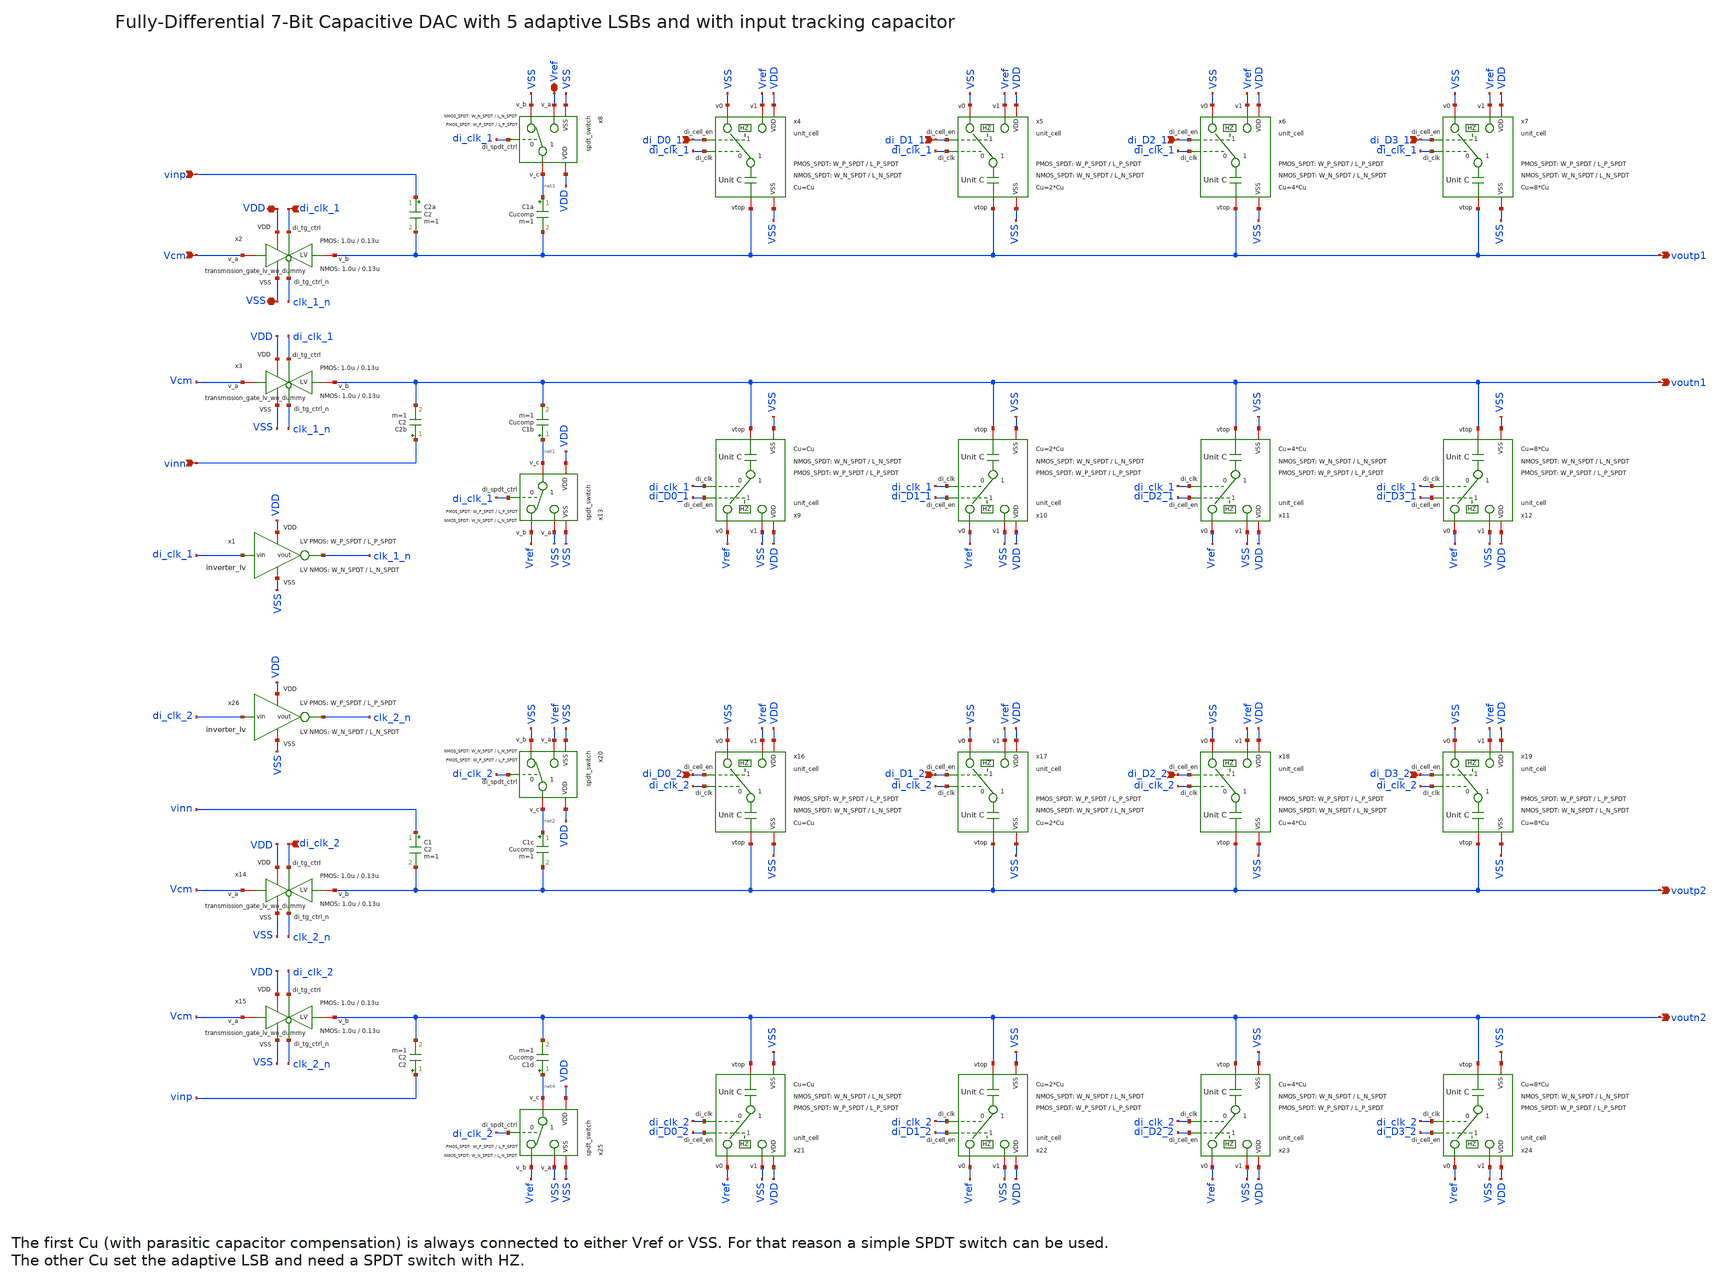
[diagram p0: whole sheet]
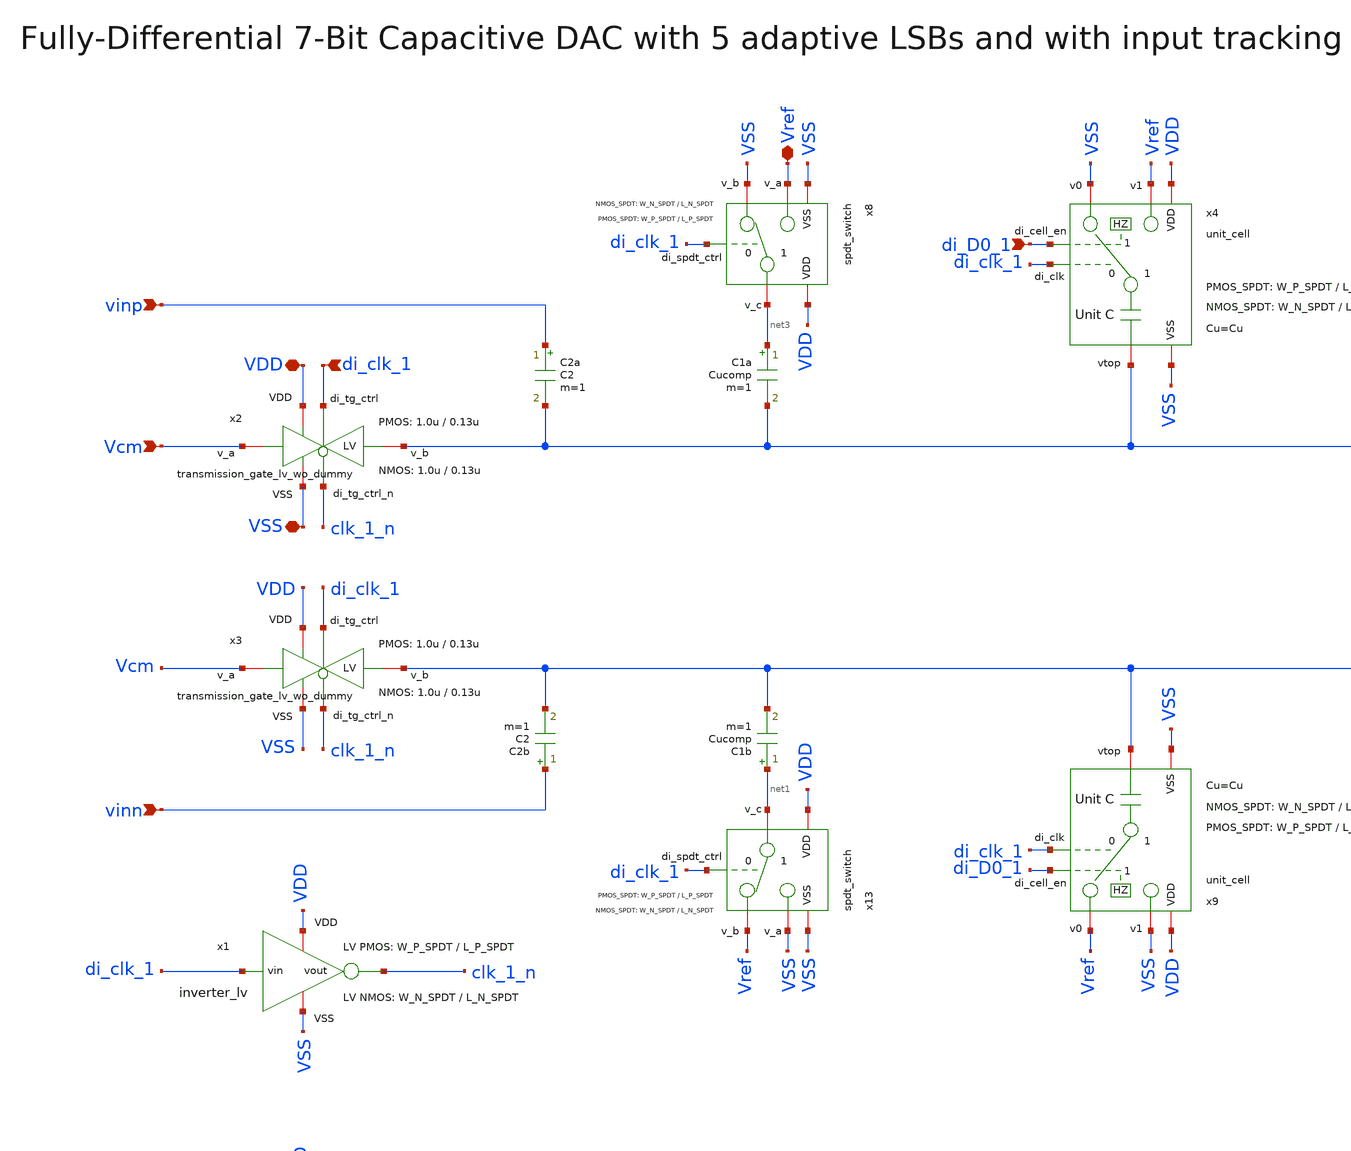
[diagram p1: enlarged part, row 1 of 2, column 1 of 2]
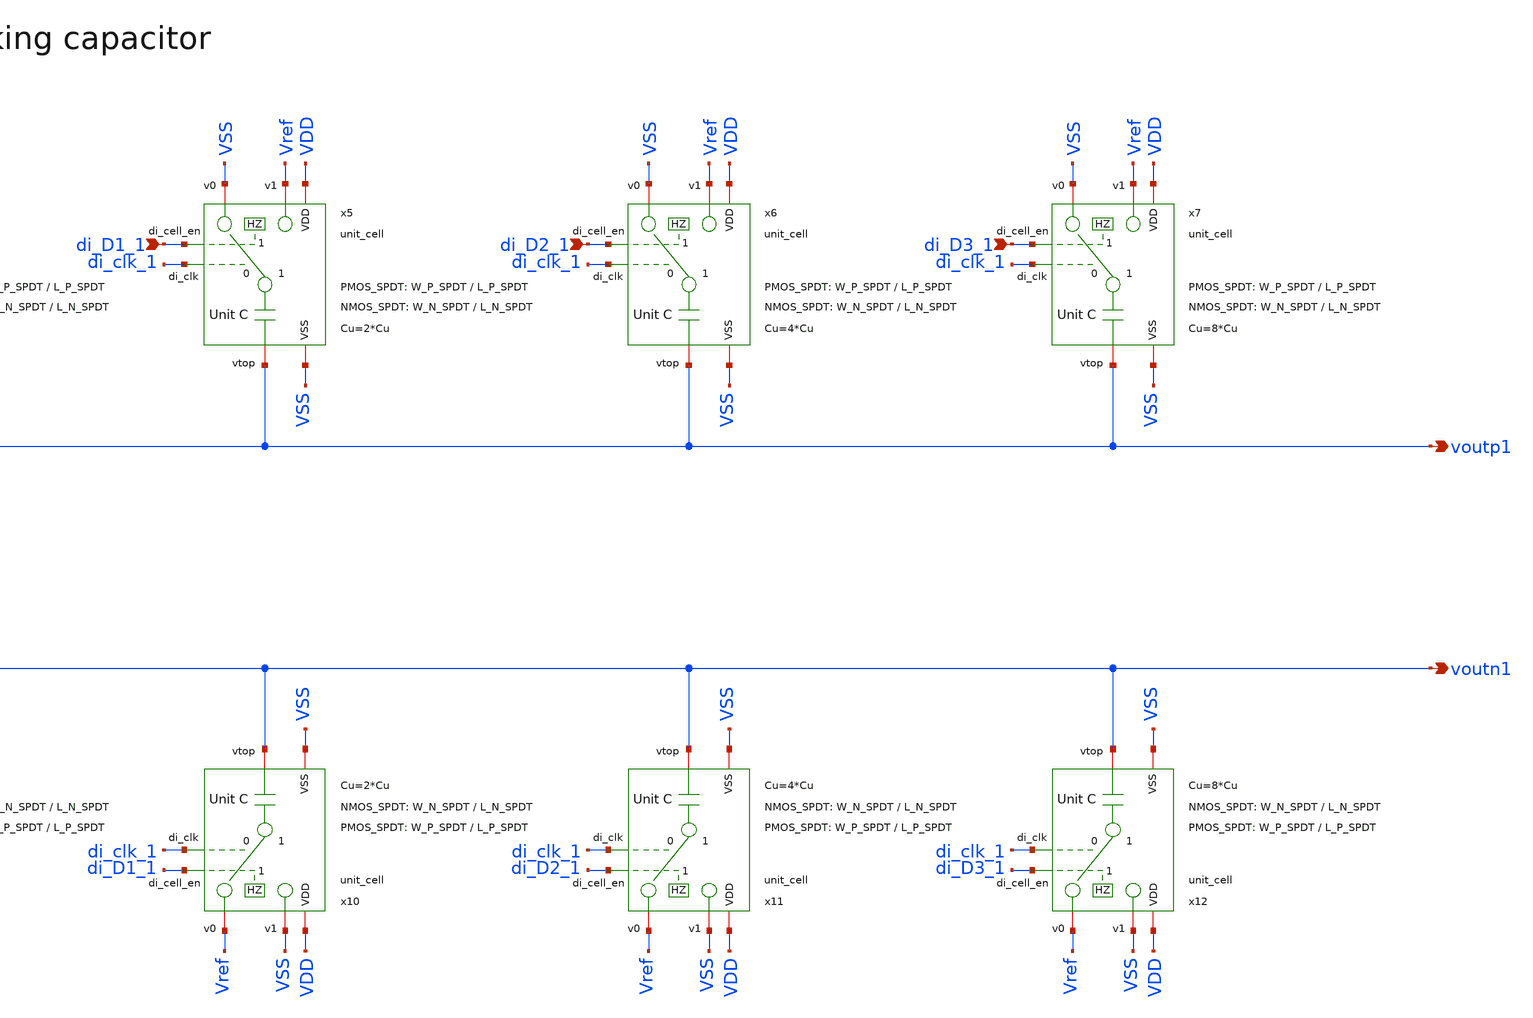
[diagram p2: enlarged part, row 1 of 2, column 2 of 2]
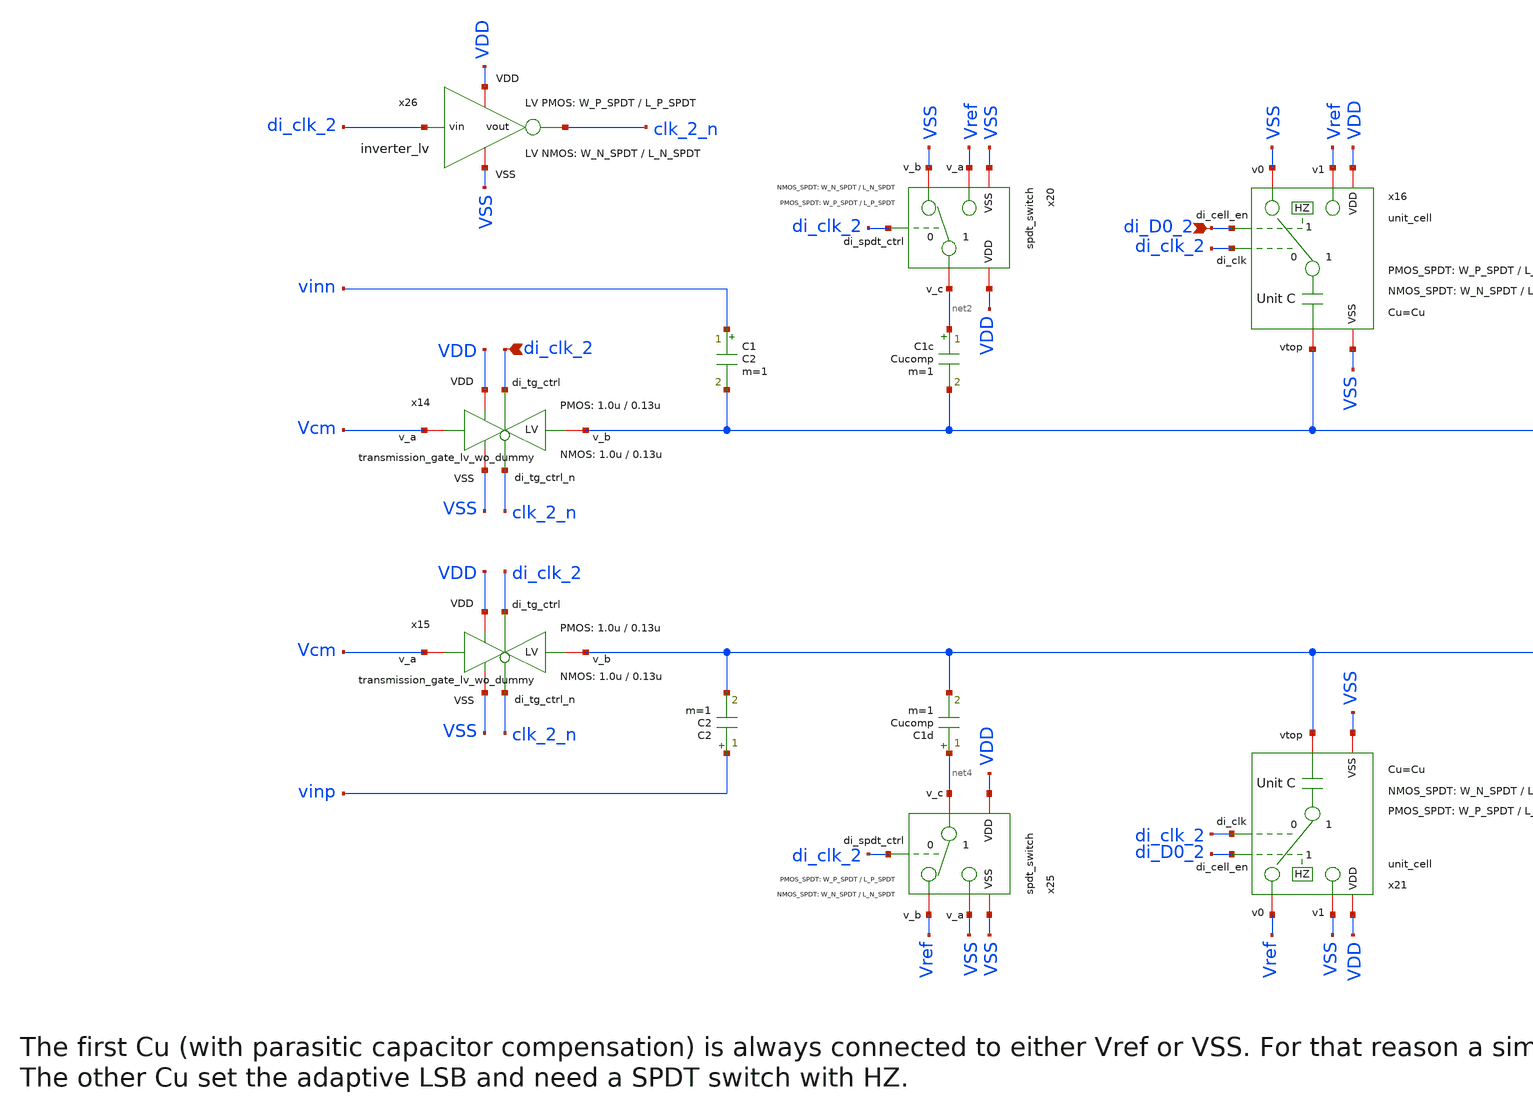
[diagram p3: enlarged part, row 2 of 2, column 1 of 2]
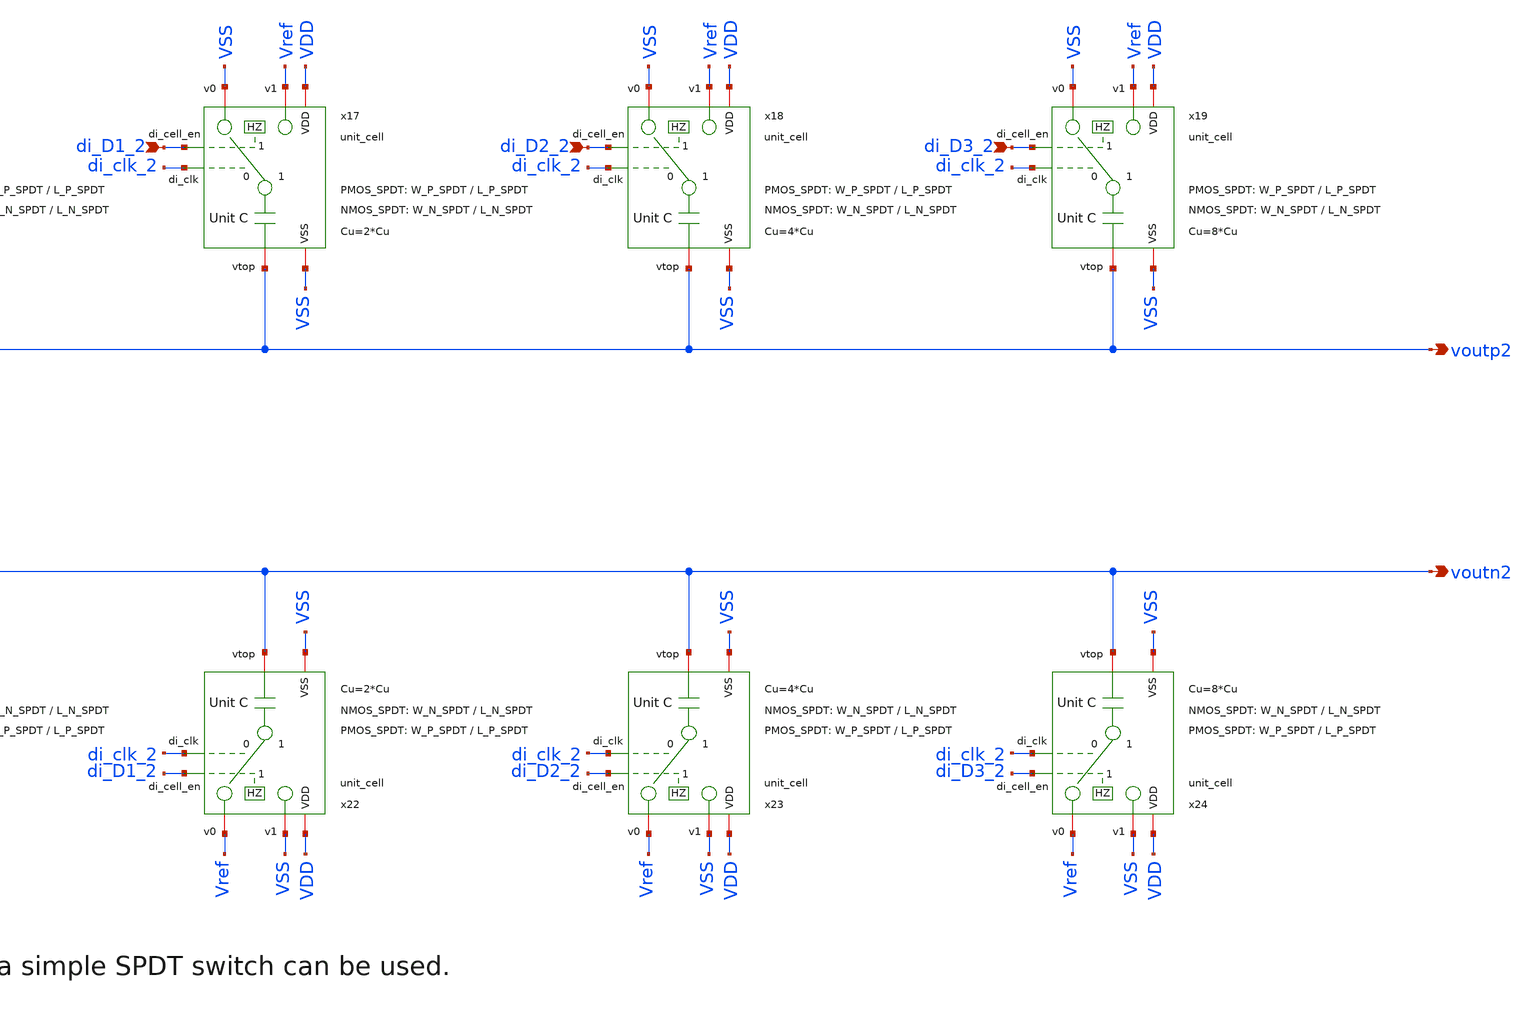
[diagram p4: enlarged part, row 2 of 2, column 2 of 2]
** sch_path: SG13G2_ATBS-ADC-main/xschem/dac/dac.sch
**.subckt dac voutp1 di_D0_1 VSS Vref voutn1 vinp vinn di_D1_1 di_D2_1 di_D3_1 voutp2 voutn2 VDD Vcm
*+ di_clk_1 di_D3_2 di_D2_2 di_D1_2 di_D0_2 di_clk_2
*.opin voutp1
*.ipin di_D0_1
*.iopin VSS
*.iopin Vref
*.opin voutn1
*.ipin vinp
*.ipin vinn
*.ipin di_D1_1
*.ipin di_D2_1
*.ipin di_D3_1
*.opin voutp2
*.opin voutn2
*.iopin VDD
*.ipin Vcm
*.ipin di_clk_1
*.ipin di_D3_2
*.ipin di_D2_2
*.ipin di_D1_2
*.ipin di_D0_2
*.ipin di_clk_2
C2a vinp voutp1 C2 m=1
C2b vinn voutn1 C2 m=1
C1a net3 voutp1 Cucomp m=1
C1b net1 voutn1 Cucomp m=1
x2 VDD di_clk_1 VSS voutp1 Vcm clk_1_n transmission_gate_lv_wo_dummy W_P=1.0u L_P=0.13u W_N=1.0u
+ L_N=0.13u
x3 VDD di_clk_1 VSS voutn1 Vcm clk_1_n transmission_gate_lv_wo_dummy W_P=1.0u L_P=0.13u W_N=1.0u
+ L_N=0.13u
x1 VDD di_clk_1 clk_1_n VSS inverter_lv W_P=W_P_SPDT L_P=L_P_SPDT W_N=W_N_SPDT L_N=L_N_SPDT
x5 Vref VSS VSS di_D1_1 di_clk_1 VDD voutp1 unit_cell W_P_SPDT=W_P_SPDT L_P_SPDT=L_P_SPDT
+ W_N_SPDT=W_N_SPDT L_N_SPDT=L_N_SPDT Cu=2*Cu
x6 Vref VSS VSS di_D2_1 di_clk_1 VDD voutp1 unit_cell W_P_SPDT=W_P_SPDT L_P_SPDT=L_P_SPDT
+ W_N_SPDT=W_N_SPDT L_N_SPDT=L_N_SPDT Cu=4*Cu
x4 Vref VSS VSS di_D0_1 di_clk_1 VDD voutp1 unit_cell W_P_SPDT=W_P_SPDT L_P_SPDT=L_P_SPDT
+ W_N_SPDT=W_N_SPDT L_N_SPDT=L_N_SPDT Cu=Cu
x7 Vref VSS VSS di_D3_1 di_clk_1 VDD voutp1 unit_cell W_P_SPDT=W_P_SPDT L_P_SPDT=L_P_SPDT
+ W_N_SPDT=W_N_SPDT L_N_SPDT=L_N_SPDT Cu=8*Cu
x9 VSS Vref VSS di_D0_1 di_clk_1 VDD voutn1 unit_cell W_P_SPDT=W_P_SPDT L_P_SPDT=L_P_SPDT
+ W_N_SPDT=W_N_SPDT L_N_SPDT=L_N_SPDT Cu=Cu
x10 VSS Vref VSS di_D1_1 di_clk_1 VDD voutn1 unit_cell W_P_SPDT=W_P_SPDT L_P_SPDT=L_P_SPDT
+ W_N_SPDT=W_N_SPDT L_N_SPDT=L_N_SPDT Cu=2*Cu
x11 VSS Vref VSS di_D2_1 di_clk_1 VDD voutn1 unit_cell W_P_SPDT=W_P_SPDT L_P_SPDT=L_P_SPDT
+ W_N_SPDT=W_N_SPDT L_N_SPDT=L_N_SPDT Cu=4*Cu
x12 VSS Vref VSS di_D3_1 di_clk_1 VDD voutn1 unit_cell W_P_SPDT=W_P_SPDT L_P_SPDT=L_P_SPDT
+ W_N_SPDT=W_N_SPDT L_N_SPDT=L_N_SPDT Cu=8*Cu
C1 vinn voutp2 C2 m=1
C2 vinp voutn2 C2 m=1
C1c net2 voutp2 Cucomp m=1
C1d net4 voutn2 Cucomp m=1
x14 VDD di_clk_2 VSS voutp2 Vcm clk_2_n transmission_gate_lv_wo_dummy W_P=1.0u L_P=0.13u W_N=1.0u
+ L_N=0.13u
x15 VDD di_clk_2 VSS voutn2 Vcm clk_2_n transmission_gate_lv_wo_dummy W_P=1.0u L_P=0.13u W_N=1.0u
+ L_N=0.13u
x17 Vref VSS VSS di_D1_2 di_clk_2 VDD voutp2 unit_cell W_P_SPDT=W_P_SPDT L_P_SPDT=L_P_SPDT
+ W_N_SPDT=W_N_SPDT L_N_SPDT=L_N_SPDT Cu=2*Cu
x18 Vref VSS VSS di_D2_2 di_clk_2 VDD voutp2 unit_cell W_P_SPDT=W_P_SPDT L_P_SPDT=L_P_SPDT
+ W_N_SPDT=W_N_SPDT L_N_SPDT=L_N_SPDT Cu=4*Cu
x16 Vref VSS VSS di_D0_2 di_clk_2 VDD voutp2 unit_cell W_P_SPDT=W_P_SPDT L_P_SPDT=L_P_SPDT
+ W_N_SPDT=W_N_SPDT L_N_SPDT=L_N_SPDT Cu=Cu
x19 Vref VSS VSS di_D3_2 di_clk_2 VDD voutp2 unit_cell W_P_SPDT=W_P_SPDT L_P_SPDT=L_P_SPDT
+ W_N_SPDT=W_N_SPDT L_N_SPDT=L_N_SPDT Cu=8*Cu
x21 VSS Vref VSS di_D0_2 di_clk_2 VDD voutn2 unit_cell W_P_SPDT=W_P_SPDT L_P_SPDT=L_P_SPDT
+ W_N_SPDT=W_N_SPDT L_N_SPDT=L_N_SPDT Cu=Cu
x22 VSS Vref VSS di_D1_2 di_clk_2 VDD voutn2 unit_cell W_P_SPDT=W_P_SPDT L_P_SPDT=L_P_SPDT
+ W_N_SPDT=W_N_SPDT L_N_SPDT=L_N_SPDT Cu=2*Cu
x23 VSS Vref VSS di_D2_2 di_clk_2 VDD voutn2 unit_cell W_P_SPDT=W_P_SPDT L_P_SPDT=L_P_SPDT
+ W_N_SPDT=W_N_SPDT L_N_SPDT=L_N_SPDT Cu=4*Cu
x24 VSS Vref VSS di_D3_2 di_clk_2 VDD voutn2 unit_cell W_P_SPDT=W_P_SPDT L_P_SPDT=L_P_SPDT
+ W_N_SPDT=W_N_SPDT L_N_SPDT=L_N_SPDT Cu=8*Cu
x8 VDD di_clk_1 VSS net3 VSS Vref spdt_switch W_P_TG=W_P_SPDT L_P_TG=L_P_SPDT W_N_TG=W_N_SPDT
+ L_N_TG=L_N_SPDT
x13 VDD di_clk_1 VSS net1 Vref VSS spdt_switch W_P_TG=W_P_SPDT L_P_TG=L_P_SPDT W_N_TG=W_N_SPDT
+ L_N_TG=L_N_SPDT
x20 VDD di_clk_2 VSS net2 VSS Vref spdt_switch W_P_TG=W_P_SPDT L_P_TG=L_P_SPDT W_N_TG=W_N_SPDT
+ L_N_TG=L_N_SPDT
x25 VDD di_clk_2 VSS net4 Vref VSS spdt_switch W_P_TG=W_P_SPDT L_P_TG=L_P_SPDT W_N_TG=W_N_SPDT
+ L_N_TG=L_N_SPDT
x26 VDD di_clk_2 clk_2_n VSS inverter_lv W_P=W_P_SPDT L_P=L_P_SPDT W_N=W_N_SPDT L_N=L_N_SPDT
**.ends

* expanding   symbol:  transmission_gate/transmission_gate_lv_wo_dummy.sym # of pins=6
** sym_path: SG13G2_ATBS-ADC-main/xschem/transmission_gate/transmission_gate_lv_wo_dummy.sym
** sch_path: SG13G2_ATBS-ADC-main/xschem/transmission_gate/transmission_gate_lv_wo_dummy.sch
.subckt transmission_gate_lv_wo_dummy VDD di_tg_ctrl VSS v_b v_a di_tg_ctrl_n  W_P=1.0u L_P=0.13u
+ W_N=1.0u L_N=0.13u
*.iopin v_a
*.iopin v_b
*.iopin VDD
*.iopin VSS
*.ipin di_tg_ctrl
*.ipin di_tg_ctrl_n
XM1 v_a di_tg_ctrl v_b VSS sg13_lv_nmos w=W_N l=L_N ng=1 m=1 mm_ok=1
XM2 v_a di_tg_ctrl_n v_b VDD sg13_lv_pmos w=W_P l=L_P ng=1 m=1 mm_ok=1
.ends


* expanding   symbol:  inverter/inverter_lv.sym # of pins=4
** sym_path: SG13G2_ATBS-ADC-main/xschem/inverter/inverter_lv.sym
** sch_path: SG13G2_ATBS-ADC-main/xschem/inverter/inverter_lv.sch
.subckt inverter_lv VDD vin vout VSS  W_P=3.0u L_P=0.13u W_N=1.0u L_N=0.13u
*.ipin vin
*.iopin VDD
*.iopin VSS
*.opin vout
XM1 vout vin VDD VDD sg13_lv_pmos w=W_P l=L_P ng=1 m=1 mm_ok=1
XM2 vout vin VSS VSS sg13_lv_nmos w=W_N l=L_N ng=1 m=1 mm_ok=1
.ends


* expanding   symbol:  dac/unit_cell.sym # of pins=7
** sym_path: SG13G2_ATBS-ADC-main/xschem/dac/unit_cell.sym
** sch_path: SG13G2_ATBS-ADC-main/xschem/dac/unit_cell.sch
.subckt unit_cell v1 v0 VSS di_cell_en di_clk VDD vtop  W_P_SPDT=1.0u L_P_SPDT=0.13u W_N_SPDT=1.0u
+ L_N_SPDT=0.13u Cu=8f
*.ipin di_cell_en
*.iopin VSS
*.iopin v0
*.iopin VDD
*.ipin di_clk
*.iopin v1
*.iopin vtop
x1 VDD di_clk VSS net1 v0 v1 di_cell_en_n spdt_hz_switch W_P_TG=W_P_SPDT L_P_TG=L_P_SPDT
+ W_N_TG=W_N_SPDT L_N_TG=L_N_SPDT
C1 net1 vtop Cu m=1
x3 VDD di_cell_en di_cell_en_n VSS inverter_lv W_P=W_P_SPDT L_P=W_P_SPDT W_N=W_N_SPDT L_N=W_N_SPDT
.ends


* expanding   symbol:  spdt_switch/spdt_switch.sym # of pins=6
** sym_path: SG13G2_ATBS-ADC-main/xschem/spdt_switch/spdt_switch.sym
** sch_path: SG13G2_ATBS-ADC-main/xschem/spdt_switch/spdt_switch.sch
.subckt spdt_switch VDD di_spdt_ctrl VSS v_c v_b v_a  W_P_TG=3.0u L_P_TG=0.13u W_N_TG=1.0u
+ L_N_TG=0.13u
*.iopin v_a
*.iopin v_b
*.iopin v_c
*.iopin VDD
*.iopin VSS
*.ipin di_spdt_ctrl
x1 VDD di_spdt_ctrl VSS v_c v_a di_spdt_ctrl_n transmission_gate_lv_wo_dummy W_P=W_P_TG L_P=L_P_TG
+ W_N=W_N_TG L_N=L_N_TG
x2 VDD di_spdt_ctrl_n VSS v_b v_c di_spdt_ctrl transmission_gate_lv_wo_dummy W_P=W_P_TG L_P=L_P_TG
+ W_N=W_N_TG L_N=L_N_TG
x8 VDD di_spdt_ctrl di_spdt_ctrl_n VSS inverter_lv W_P=W_P_TG L_P=L_P_TG W_N=W_N_TG L_N=L_N_TG
.ends


* expanding   symbol:  spdt_switch/spdt_hz_switch.sym # of pins=7
** sym_path: SG13G2_ATBS-ADC-main/xschem/spdt_switch/spdt_hz_switch.sym
** sch_path: SG13G2_ATBS-ADC-main/xschem/spdt_switch/spdt_hz_switch.sch
.subckt spdt_hz_switch VDD di_spdt_ctrl VSS v_c v_b v_a di_spdt_hz  W_P_TG=3.0u L_P_TG=0.13u
+ W_N_TG=1.0u L_N_TG=0.13u
*.iopin v_a
*.iopin v_b
*.iopin v_c
*.iopin VDD
*.iopin VSS
*.ipin di_spdt_ctrl
*.ipin di_spdt_hz
x1 VDD di_spdt_ctrl VSS net1 v_a di_spdt_ctrl_n transmission_gate_lv_wo_dummy W_P=W_P_TG L_P=L_P_TG
+ W_N=W_N_TG L_N=L_N_TG
x2 VDD di_spdt_ctrl_n VSS v_b net1 di_spdt_ctrl transmission_gate_lv_wo_dummy W_P=W_P_TG L_P=L_P_TG
+ W_N=W_N_TG L_N=L_N_TG
x8 VDD di_spdt_ctrl di_spdt_ctrl_n VSS inverter_lv W_P=W_P_TG L_P=L_P_TG W_N=W_N_TG L_N=L_N_TG
x3 VDD di_spdt_hz di_spdt_hz_n VSS inverter_lv W_P=W_P_TG L_P=L_P_TG W_N=W_N_TG L_N=L_N_TG
x4 VDD di_spdt_hz_n VSS v_c net1 di_spdt_hz transmission_gate_lv_wo_dummy W_P=W_P_TG L_P=L_P_TG
+ W_N=W_N_TG L_N=L_N_TG
.ends

.end
